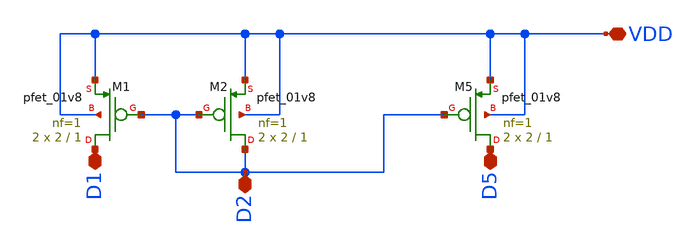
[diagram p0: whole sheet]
** sch_path: opamp/mag/pmos.sch
**.subckt pmos VDD D5 D2 D1
*.iopin VDD
*.iopin D5
*.iopin D2
*.iopin D1
XM1 D1 D2 VDD VDD sky130_fd_pr__pfet_01v8 L=1 W=2 nf=1 ad='int((nf+1)/2) * W/nf * 0.29' as='int((nf+2)/2) * W/nf * 0.29'
+ pd='2*int((nf+1)/2) * (W/nf + 0.29)' ps='2*int((nf+2)/2) * (W/nf + 0.29)' nrd='0.29 / W' nrs='0.29 / W'
+ sa=0 sb=0 sd=0 mult=2 m=2
XM2 D2 D2 VDD VDD sky130_fd_pr__pfet_01v8 L=1 W=2 nf=1 ad='int((nf+1)/2) * W/nf * 0.29' as='int((nf+2)/2) * W/nf * 0.29'
+ pd='2*int((nf+1)/2) * (W/nf + 0.29)' ps='2*int((nf+2)/2) * (W/nf + 0.29)' nrd='0.29 / W' nrs='0.29 / W'
+ sa=0 sb=0 sd=0 mult=2 m=2
XM5 D5 D2 VDD VDD sky130_fd_pr__pfet_01v8 L=1 W=2 nf=1 ad='int((nf+1)/2) * W/nf * 0.29' as='int((nf+2)/2) * W/nf * 0.29'
+ pd='2*int((nf+1)/2) * (W/nf + 0.29)' ps='2*int((nf+2)/2) * (W/nf + 0.29)' nrd='0.29 / W' nrs='0.29 / W'
+ sa=0 sb=0 sd=0 mult=2 m=2
**.ends
.end
